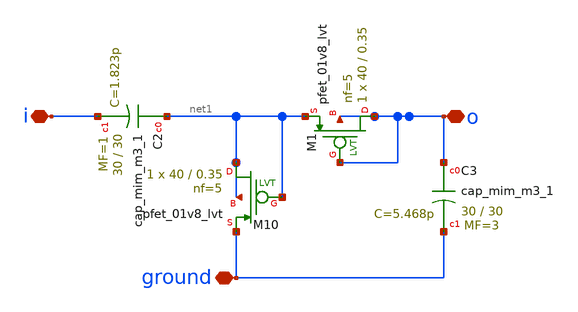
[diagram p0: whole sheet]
** sch_path: xschem/cell.sch
**.subckt cell ground o i
*.iopin ground
*.iopin o
*.iopin i
XM10 net1 net1 ground net1 sky130_fd_pr__pfet_01v8_lvt L=0.35 W=40 nf=5 ad='int((5 + 1)/2) * 40 / 5 * 0.29'
+ as='int((5 + 2)/2) * 40 / 5 * 0.29' pd='2*int((5 + 1)/2) * (40 / 5 + 0.29)' ps='2*int((5 + 2)/2) * (40 / 5 + 0.29)'
+ nrd='0.29 / 40 ' nrs='0.29 / 40 ' sa=0 sb=0 sd=0 mult=1 m=1
XM1 o o net1 o sky130_fd_pr__pfet_01v8_lvt L=0.35 W=40 nf=5 ad='int((5 + 1)/2) * 40 / 5 * 0.29' as='int((5 + 2)/2) * 40 / 5 * 0.29'
+ pd='2*int((5 + 1)/2) * (40 / 5 + 0.29)' ps='2*int((5 + 2)/2) * (40 / 5 + 0.29)' nrd='0.29 / 40 ' nrs='0.29 / 40 '
+ sa=0 sb=0 sd=0 mult=1 m=1
XC3 o ground sky130_fd_pr__cap_mim_m3_1 W=30 L=30 MF=3 m=3
XC2 net1 i sky130_fd_pr__cap_mim_m3_1 W=30 L=30 MF=1 m=1
**.ends
.end
